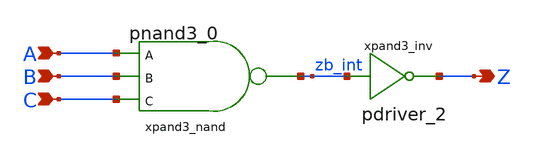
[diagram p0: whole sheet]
** sch_path: sram_4_16_scn4m/pand3_0.sch
**.subckt pand3_0 A B C Z
*.ipin A
*.ipin B
*.ipin C
*.opin Z
xpand3_nand A B C zb_int vdd gnd pnand3_0
xpand3_inv zb_int Z vdd gnd pdriver_2
**.ends

* expanding   symbol:  pnand3_0.sym # of pins=4
** sym_path: sram_4_16_scn4m/pnand3_0.sym
** sch_path: sram_4_16_scn4m/pnand3_0.sch
.subckt pnand3_0 A B C Z vdd gnd
*.ipin C
*.ipin A
*.ipin B
*.opin Z
*.iopin vdd
*.iopin gnd
XMpnand3_nmos1 Z C net1 gnd sky130_fd_pr__nfet_01v8 L=0.4 W=1.6 nf=1 ad='int((nf+1)/2) * W/nf * 0.29'
+ as='int((nf+2)/2) * W/nf * 0.29' pd='2*int((nf+1)/2) * (W/nf + 0.29)' ps='2*int((nf+2)/2) * (W/nf + 0.29)'
+ nrd='0.29 / W' nrs='0.29 / W' sa=0 sb=0 sd=0 mult=1 m=1
XMpnand3_pmos1 Z A vdd vdd sky130_fd_pr__pfet_01v8 L=0.4 W=1.6 nf=1 ad='int((nf+1)/2) * W/nf * 0.29'
+ as='int((nf+2)/2) * W/nf * 0.29' pd='2*int((nf+1)/2) * (W/nf + 0.29)' ps='2*int((nf+2)/2) * (W/nf + 0.29)'
+ nrd='0.29 / W' nrs='0.29 / W' sa=0 sb=0 sd=0 mult=1 m=1
XMpnand3_pmos3 Z C vdd vdd sky130_fd_pr__pfet_01v8 L=0.4 W=1.6 nf=1 ad='int((nf+1)/2) * W/nf * 0.29'
+ as='int((nf+2)/2) * W/nf * 0.29' pd='2*int((nf+1)/2) * (W/nf + 0.29)' ps='2*int((nf+2)/2) * (W/nf + 0.29)'
+ nrd='0.29 / W' nrs='0.29 / W' sa=0 sb=0 sd=0 mult=1 m=1
XMpnand3_nmos2 net1 B net2 gnd sky130_fd_pr__nfet_01v8 L=0.4 W=1.6 nf=1 ad='int((nf+1)/2) * W/nf * 0.29'
+ as='int((nf+2)/2) * W/nf * 0.29' pd='2*int((nf+1)/2) * (W/nf + 0.29)' ps='2*int((nf+2)/2) * (W/nf + 0.29)'
+ nrd='0.29 / W' nrs='0.29 / W' sa=0 sb=0 sd=0 mult=1 m=1
XMpnand3_pmos2 Z B vdd vdd sky130_fd_pr__pfet_01v8 L=0.4 W=1.6 nf=1 ad='int((nf+1)/2) * W/nf * 0.29'
+ as='int((nf+2)/2) * W/nf * 0.29' pd='2*int((nf+1)/2) * (W/nf + 0.29)' ps='2*int((nf+2)/2) * (W/nf + 0.29)'
+ nrd='0.29 / W' nrs='0.29 / W' sa=0 sb=0 sd=0 mult=1 m=1
XMpnand3_nmos3 net2 A gnd gnd sky130_fd_pr__nfet_01v8 L=0.4 W=1.6 nf=1 ad='int((nf+1)/2) * W/nf * 0.29'
+ as='int((nf+2)/2) * W/nf * 0.29' pd='2*int((nf+1)/2) * (W/nf + 0.29)' ps='2*int((nf+2)/2) * (W/nf + 0.29)'
+ nrd='0.29 / W' nrs='0.29 / W' sa=0 sb=0 sd=0 mult=1 m=1
.ends


* expanding   symbol:  pdriver_2.sym # of pins=2
** sym_path: sram_4_16_scn4m/pdriver_2.sym
** sch_path: sram_4_16_scn4m/pdriver_2.sch
.subckt pdriver_2 A Z vdd gnd
*.ipin A
*.opin Z
xbuf_inv1 A Z vdd gnd pinv_11
.ends


* expanding   symbol:  pinv_11.sym # of pins=2
** sym_path: sram_4_16_scn4m/pinv_11.sym
** sch_path: sram_4_16_scn4m/pinv_11.sch
.subckt pinv_11 A Z vdd gnd
*.ipin A
*.opin Z
*.iopin vdd
*.iopin gnd
XM2 Z A gnd gnd sky130_fd_pr__nfet_01v8 L=0.4 W=3.2 nf=1 ad='int((nf+1)/2) * W/nf * 0.29' as='int((nf+2)/2) * W/nf * 0.29'
+ pd='2*int((nf+1)/2) * (W/nf + 0.29)' ps='2*int((nf+2)/2) * (W/nf + 0.29)' nrd='0.29 / W' nrs='0.29 / W'
+ sa=0 sb=0 sd=0 mult=1 m=1
XM3 Z A vdd vdd sky130_fd_pr__pfet_01v8 L=0.4 W=6.4 nf=1 ad='int((nf+1)/2) * W/nf * 0.29' as='int((nf+2)/2) * W/nf * 0.29'
+ pd='2*int((nf+1)/2) * (W/nf + 0.29)' ps='2*int((nf+2)/2) * (W/nf + 0.29)' nrd='0.29 / W' nrs='0.29 / W'
+ sa=0 sb=0 sd=0 mult=1 m=1
.ends

.end
